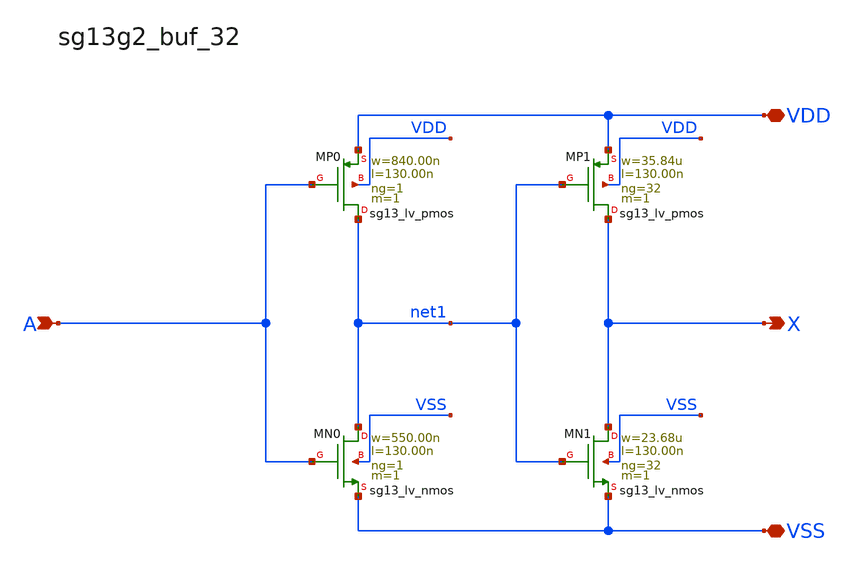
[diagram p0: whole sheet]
** sch_path: outputs/sg13g2_cells/cells/sg13g2_buf_32/sg13g2_buf_32.sch
**.subckt sg13g2_buf_32 X A VDD VSS
*.opin X
*.ipin A
*.iopin VDD
*.iopin VSS
XMN0 net1 A VSS VSS sg13_lv_nmos w=550.00n l=130.00n ng=1 m=1 mm_ok=1
XMN1 X net1 VSS VSS sg13_lv_nmos w=23.68u l=130.00n ng=32 m=1 mm_ok=1
XMP1 X net1 VDD VDD sg13_lv_pmos w=35.84u l=130.00n ng=32 m=1 mm_ok=1
XMP0 net1 A VDD VDD sg13_lv_pmos w=840.00n l=130.00n ng=1 m=1 mm_ok=1
**.ends
.end
